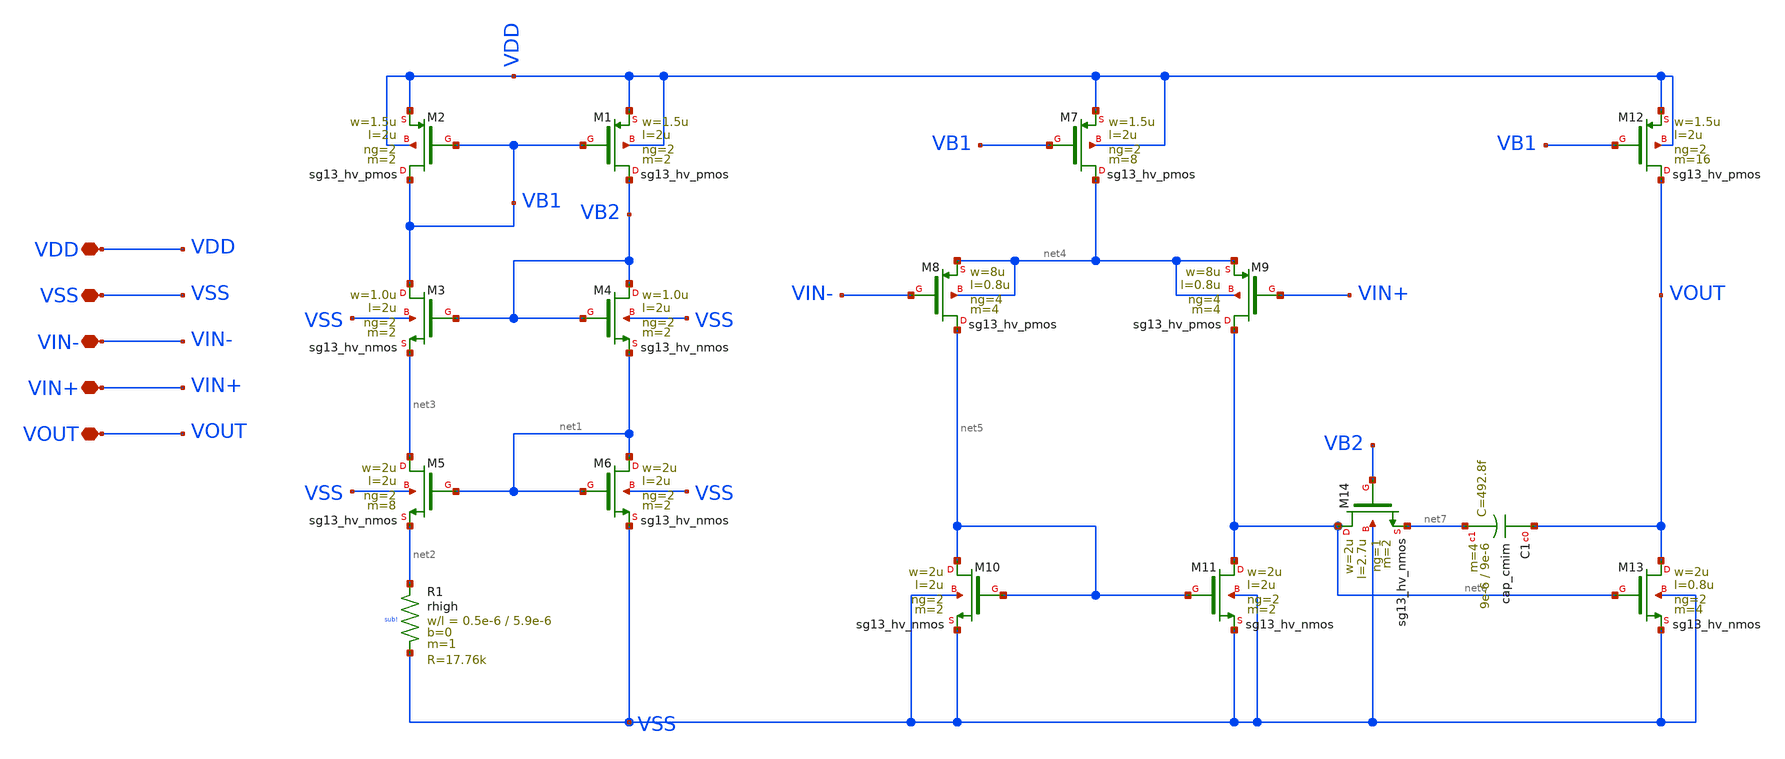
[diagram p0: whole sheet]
** sch_path: LIB/ihp-sg13g2/Amplifiers/Va001_ihp-sg13g2_3_3.sch
**.subckt Va001_ihp-sg13g2_3_3 VDD VSS VIN- VIN+ VOUT
*.iopin VDD
*.iopin VSS
*.iopin VIN-
*.iopin VIN+
*.iopin VOUT
XM2 VB1 VB1 VDD VDD sg13_hv_pmos w=1.5u l=2u ng=2 m=2 mm_ok=1
XM1 VB2 VB1 VDD VDD sg13_hv_pmos w=1.5u l=2u ng=2 m=2 mm_ok=1
XM3 VB1 VB2 net3 VSS sg13_hv_nmos w=1.0u l=2u ng=2 m=2 mm_ok=1
XM4 VB2 VB2 net1 VSS sg13_hv_nmos w=1.0u l=2u ng=2 m=2 mm_ok=1
XM5 net3 net1 net2 VSS sg13_hv_nmos w=2u l=2u ng=2 m=8 mm_ok=1
XM6 net1 net1 VSS VSS sg13_hv_nmos w=2u l=2u ng=2 m=2 mm_ok=1
XR1 net2 VSS sub! rhigh w=0.5e-6 l=5.9e-6 m=1 b=0 mm_ok=1
XM7 net4 VB1 VDD VDD sg13_hv_pmos w=1.5u l=2u ng=2 m=8 mm_ok=1
XM9 net6 VIN+ net4 net4 sg13_hv_pmos w=8u l=0.8u ng=4 m=4 mm_ok=1
XM8 net5 VIN- net4 net4 sg13_hv_pmos w=8u l=0.8u ng=4 m=4 mm_ok=1
XM10 net5 net5 VSS VSS sg13_hv_nmos w=2u l=2u ng=2 m=2 mm_ok=1
XM11 net6 net5 VSS VSS sg13_hv_nmos w=2u l=2u ng=2 m=2 mm_ok=1
XM12 VOUT VB1 VDD VDD sg13_hv_pmos w=1.5u l=2u ng=2 m=16 mm_ok=1
XM13 VOUT net6 VSS VSS sg13_hv_nmos w=2u l=0.8u ng=2 m=4 mm_ok=1
XM14 net6 VB2 net7 VSS sg13_hv_nmos w=2u l=2.7u ng=1 m=2 mm_ok=1
XC1 VOUT net7 cap_cmim w=9e-6 l=9e-6 m=4 mm_ok=1
**.ends
.end
